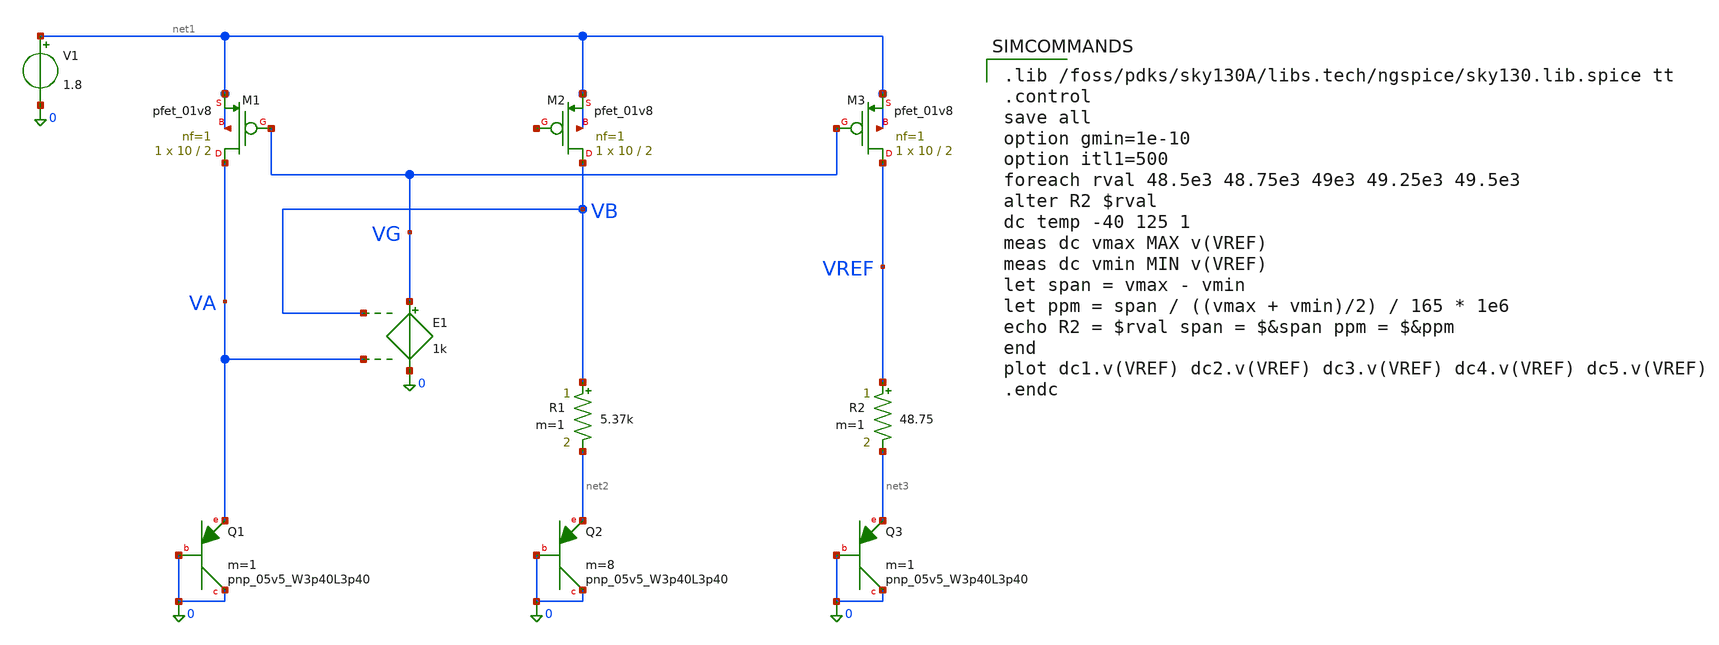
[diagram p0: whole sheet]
** sch_path: bandgap_ideal.sch
**.subckt bandgap_ideal
XM1 VA VG net1 net1 sky130_fd_pr__pfet_01v8 L=2 W=10 nf=1 ad='int((1 + 1)/2) * 10 / 1 * 0.29' as='int((1 + 2)/2) * 10 / 1 * 0.29'
+ pd='2*int((1 + 1)/2) * (10 / 1 + 0.29)' ps='2*int((1 + 2)/2) * (10 / 1 + 0.29)' nrd='0.29 / 10 ' nrs='0.29 / 10 '
+ sa=0 sb=0 sd=0 mult=1 m=1
XM2 VB net4 net1 net1 sky130_fd_pr__pfet_01v8 L=2 W=10 nf=1 ad='int((1 + 1)/2) * 10 / 1 * 0.29' as='int((1 + 2)/2) * 10 / 1 * 0.29'
+ pd='2*int((1 + 1)/2) * (10 / 1 + 0.29)' ps='2*int((1 + 2)/2) * (10 / 1 + 0.29)' nrd='0.29 / 10 ' nrs='0.29 / 10 '
+ sa=0 sb=0 sd=0 mult=1 m=1
XM3 VREF VG net1 net1 sky130_fd_pr__pfet_01v8 L=2 W=10 nf=1 ad='int((1 + 1)/2) * 10 / 1 * 0.29' as='int((1 + 2)/2) * 10 / 1 * 0.29'
+ pd='2*int((1 + 1)/2) * (10 / 1 + 0.29)' ps='2*int((1 + 2)/2) * (10 / 1 + 0.29)' nrd='0.29 / 10 ' nrs='0.29 / 10 '
+ sa=0 sb=0 sd=0 mult=1 m=1
XQ1 0 0 VA sky130_fd_pr__pnp_05v5_W3p40L3p40 m=1
XQ2 0 0 net2 sky130_fd_pr__pnp_05v5_W3p40L3p40 m=8
XQ3 0 0 net3 sky130_fd_pr__pnp_05v5_W3p40L3p40 m=1
R1 VB net2 5.37k m=1
R2 VREF net3 48.75 m=1
V1 net1 0 1.8
E1 VG 0 VB VA 1k
**** begin user architecture code

.lib /foss/pdks/sky130A/libs.tech/ngspice/sky130.lib.spice tt
.control
save all
option gmin=1e-10
option itl1=500
foreach rval 48.5e3 48.75e3 49e3 49.25e3 49.5e3
alter R2 $rval
dc temp -40 125 1
meas dc vmax MAX v(VREF)
meas dc vmin MIN v(VREF)
let span = vmax - vmin
let ppm = span / ((vmax + vmin)/2) / 165 * 1e6
echo R2 = $rval span = $&span ppm = $&ppm
end
plot dc1.v(VREF) dc2.v(VREF) dc3.v(VREF) dc4.v(VREF) dc5.v(VREF)
.endc

**** end user architecture code
**.ends
.end
